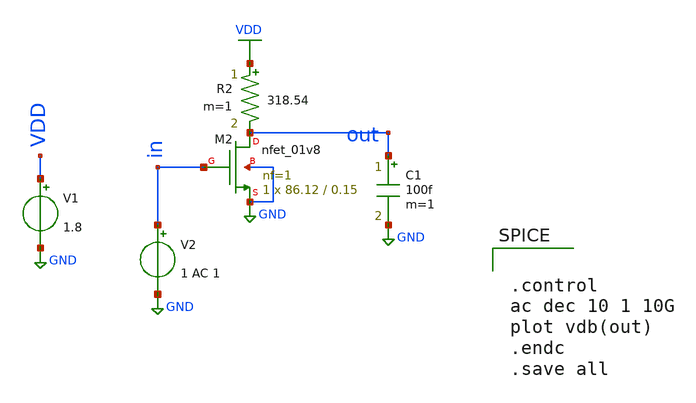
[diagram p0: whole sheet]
** sch_path: #1_cs5ghz/cs5ghz.sch
**.subckt cs5ghz
XM2 out in GND GND sky130_fd_pr__nfet_01v8 L=0.15 W=86.12 nf=1 ad='int((1 + 1)/2) * 86.12 / 1 * 0.29'
+ as='int((1 + 2)/2) * 86.12 / 1 * 0.29' pd='2*int((1 + 1)/2) * (86.12 / 1 + 0.29)' ps='2*int((1 + 2)/2) * (86.12 / 1 + 0.29)'
+ nrd='0.29 / 86.12 ' nrs='0.29 / 86.12 ' sa=0 sb=0 sd=0 mult=1 m=1
V1 VDD GND 1.8
R2 VDD out 318.54 m=1
V2 in GND 1 AC 1
C1 out GND 100f m=1
**** begin user architecture code

** opencircuitdesign pdks install
.lib $::SKYWATER_MODELS/sky130.lib.spice tt




.control
ac dec 10 1 10G
plot vdb(out)
.endc
.save all


**** end user architecture code
**.ends
.GLOBAL GND
.GLOBAL VDD
.end
